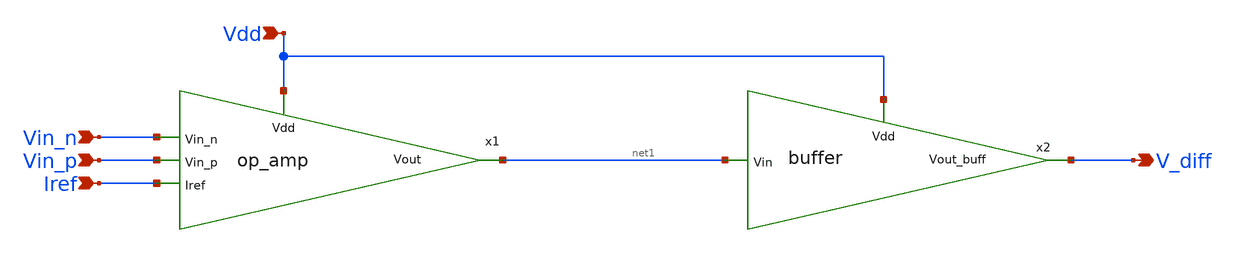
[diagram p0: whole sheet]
** sch_path: blocks/adc/lvds/lvds_rec_v3.sch
**.subckt lvds_rec_v3 Vin_p Vin_n V_diff Iref Vdd
*.ipin Vin_p
*.ipin Vin_n
*.opin V_diff
*.ipin Iref
*.ipin Vdd
x1 Vdd net1 Vin_n Vin_p Iref op_amp
x2 Vdd V_diff net1 buffer
**.ends

* expanding   symbol:  op_amp.sym # of pins=5
** sym_path: blocks/adc/lvds/op_amp.sym
** sch_path: blocks/adc/lvds/op_amp.sch
.subckt op_amp Vdd Vout Vin_n Vin_p Iref
*.ipin Vdd
*.ipin Vin_p
*.ipin Vin_n
*.opin Vout
*.ipin Iref
XM1 net2 net3 Vdd Vdd pfet_03v3 L=0.28u W=10.5u nf=1 ad='int((nf+1)/2) * W/nf * 0.18u' as='int((nf+2)/2) * W/nf * 0.18u'
+ pd='2*int((nf+1)/2) * (W/nf + 0.18u)' ps='2*int((nf+2)/2) * (W/nf + 0.18u)' nrd='0.18u / W' nrs='0.18u / W'
+ sa=0 sb=0 sd=0 m=1
XM2 net1 net4 Vdd Vdd pfet_03v3 L=0.28u W=10.5u nf=1 ad='int((nf+1)/2) * W/nf * 0.18u' as='int((nf+2)/2) * W/nf * 0.18u'
+ pd='2*int((nf+1)/2) * (W/nf + 0.18u)' ps='2*int((nf+2)/2) * (W/nf + 0.18u)' nrd='0.18u / W' nrs='0.18u / W'
+ sa=0 sb=0 sd=0 m=1
XM3 net3 Vb2 net2 Vdd pfet_03v3 L=0.28u W=10.5u nf=1 ad='int((nf+1)/2) * W/nf * 0.18u' as='int((nf+2)/2) * W/nf * 0.18u'
+ pd='2*int((nf+1)/2) * (W/nf + 0.18u)' ps='2*int((nf+2)/2) * (W/nf + 0.18u)' nrd='0.18u / W' nrs='0.18u / W'
+ sa=0 sb=0 sd=0 m=1
XM4 net4 Vb2 net1 Vdd pfet_03v3 L=0.28u W=10.5u nf=1 ad='int((nf+1)/2) * W/nf * 0.18u' as='int((nf+2)/2) * W/nf * 0.18u'
+ pd='2*int((nf+1)/2) * (W/nf + 0.18u)' ps='2*int((nf+2)/2) * (W/nf + 0.18u)' nrd='0.18u / W' nrs='0.18u / W'
+ sa=0 sb=0 sd=0 m=1
XM5 net4 Vin_p net5 0 nfet_03v3 L=0.28u W=52.5u nf=15 ad='int((nf+1)/2) * W/nf * 0.18u' as='int((nf+2)/2) * W/nf * 0.18u'
+ pd='2*int((nf+1)/2) * (W/nf + 0.18u)' ps='2*int((nf+2)/2) * (W/nf + 0.18u)' nrd='0.18u / W' nrs='0.18u / W'
+ sa=0 sb=0 sd=0 m=1
XM6 net3 Vin_n net5 0 nfet_03v3 L=0.28u W=52.5u nf=15 ad='int((nf+1)/2) * W/nf * 0.18u' as='int((nf+2)/2) * W/nf * 0.18u'
+ pd='2*int((nf+1)/2) * (W/nf + 0.18u)' ps='2*int((nf+2)/2) * (W/nf + 0.18u)' nrd='0.18u / W' nrs='0.18u / W'
+ sa=0 sb=0 sd=0 m=1
XM7 net6 net4 Vdd Vdd pfet_03v3 L=0.28u W=10.5u nf=1 ad='int((nf+1)/2) * W/nf * 0.18u' as='int((nf+2)/2) * W/nf * 0.18u'
+ pd='2*int((nf+1)/2) * (W/nf + 0.18u)' ps='2*int((nf+2)/2) * (W/nf + 0.18u)' nrd='0.18u / W' nrs='0.18u / W'
+ sa=0 sb=0 sd=0 m=1
XM9 net7 net3 Vdd Vdd pfet_03v3 L=0.28u W=10.5u nf=1 ad='int((nf+1)/2) * W/nf * 0.18u' as='int((nf+2)/2) * W/nf * 0.18u'
+ pd='2*int((nf+1)/2) * (W/nf + 0.18u)' ps='2*int((nf+2)/2) * (W/nf + 0.18u)' nrd='0.18u / W' nrs='0.18u / W'
+ sa=0 sb=0 sd=0 m=1
XM11 net8 Vb2 net10 0 nfet_03v3 L=0.28u W=5.25u nf=1 ad='int((nf+1)/2) * W/nf * 0.18u' as='int((nf+2)/2) * W/nf * 0.18u'
+ pd='2*int((nf+1)/2) * (W/nf + 0.18u)' ps='2*int((nf+2)/2) * (W/nf + 0.18u)' nrd='0.18u / W' nrs='0.18u / W'
+ sa=0 sb=0 sd=0 m=1
XM12 Vout Vb2 net9 0 nfet_03v3 L=0.28u W=5.25u nf=1 ad='int((nf+1)/2) * W/nf * 0.18u' as='int((nf+2)/2) * W/nf * 0.18u'
+ pd='2*int((nf+1)/2) * (W/nf + 0.18u)' ps='2*int((nf+2)/2) * (W/nf + 0.18u)' nrd='0.18u / W' nrs='0.18u / W'
+ sa=0 sb=0 sd=0 m=1
XM13 net10 net8 0 0 nfet_03v3 L=0.28u W=5.25u nf=1 ad='int((nf+1)/2) * W/nf * 0.18u' as='int((nf+2)/2) * W/nf * 0.18u'
+ pd='2*int((nf+1)/2) * (W/nf + 0.18u)' ps='2*int((nf+2)/2) * (W/nf + 0.18u)' nrd='0.18u / W' nrs='0.18u / W'
+ sa=0 sb=0 sd=0 m=1
XM14 net9 net8 0 0 nfet_03v3 L=0.28u W=5.25u nf=1 ad='int((nf+1)/2) * W/nf * 0.18u' as='int((nf+2)/2) * W/nf * 0.18u'
+ pd='2*int((nf+1)/2) * (W/nf + 0.18u)' ps='2*int((nf+2)/2) * (W/nf + 0.18u)' nrd='0.18u / W' nrs='0.18u / W'
+ sa=0 sb=0 sd=0 m=1
XM8 net8 0 net6 Vdd pfet_03v3 L=0.28u W=10.5u nf=1 ad='int((nf+1)/2) * W/nf * 0.18u' as='int((nf+2)/2) * W/nf * 0.18u'
+ pd='2*int((nf+1)/2) * (W/nf + 0.18u)' ps='2*int((nf+2)/2) * (W/nf + 0.18u)' nrd='0.18u / W' nrs='0.18u / W'
+ sa=0 sb=0 sd=0 m=1
XM10 Vout 0 net7 Vdd pfet_03v3 L=0.28u W=10.5u nf=1 ad='int((nf+1)/2) * W/nf * 0.18u' as='int((nf+2)/2) * W/nf * 0.18u'
+ pd='2*int((nf+1)/2) * (W/nf + 0.18u)' ps='2*int((nf+2)/2) * (W/nf + 0.18u)' nrd='0.18u / W' nrs='0.18u / W'
+ sa=0 sb=0 sd=0 m=1
XM15 net5 net11 0 0 nfet_03v3 L=1u W=80u nf=20 ad='int((nf+1)/2) * W/nf * 0.18u' as='int((nf+2)/2) * W/nf * 0.18u'
+ pd='2*int((nf+1)/2) * (W/nf + 0.18u)' ps='2*int((nf+2)/2) * (W/nf + 0.18u)' nrd='0.18u / W' nrs='0.18u / W'
+ sa=0 sb=0 sd=0 m=1
XM16 Iref Iref Vdd Vdd pfet_03v3 L=1u W=20u nf=1 ad='int((nf+1)/2) * W/nf * 0.18u' as='int((nf+2)/2) * W/nf * 0.18u'
+ pd='2*int((nf+1)/2) * (W/nf + 0.18u)' ps='2*int((nf+2)/2) * (W/nf + 0.18u)' nrd='0.18u / W' nrs='0.18u / W'
+ sa=0 sb=0 sd=0 m=1
XM17 net11 Iref Vdd Vdd pfet_03v3 L=1u W=80u nf=1 ad='int((nf+1)/2) * W/nf * 0.18u' as='int((nf+2)/2) * W/nf * 0.18u'
+ pd='2*int((nf+1)/2) * (W/nf + 0.18u)' ps='2*int((nf+2)/2) * (W/nf + 0.18u)' nrd='0.18u / W' nrs='0.18u / W'
+ sa=0 sb=0 sd=0 m=1
XM18 Vb2 Iref Vdd Vdd pfet_03v3 L=1u W=20u nf=1 ad='int((nf+1)/2) * W/nf * 0.18u' as='int((nf+2)/2) * W/nf * 0.18u'
+ pd='2*int((nf+1)/2) * (W/nf + 0.18u)' ps='2*int((nf+2)/2) * (W/nf + 0.18u)' nrd='0.18u / W' nrs='0.18u / W'
+ sa=0 sb=0 sd=0 m=1
XM19 Vb2 Vb2 net12 0 nfet_03v3 L=0.28u W=30u nf=1 ad='int((nf+1)/2) * W/nf * 0.18u' as='int((nf+2)/2) * W/nf * 0.18u'
+ pd='2*int((nf+1)/2) * (W/nf + 0.18u)' ps='2*int((nf+2)/2) * (W/nf + 0.18u)' nrd='0.18u / W' nrs='0.18u / W'
+ sa=0 sb=0 sd=0 m=1
XM20 net12 net12 0 0 nfet_03v3 L=0.28u W=30u nf=1 ad='int((nf+1)/2) * W/nf * 0.18u' as='int((nf+2)/2) * W/nf * 0.18u'
+ pd='2*int((nf+1)/2) * (W/nf + 0.18u)' ps='2*int((nf+2)/2) * (W/nf + 0.18u)' nrd='0.18u / W' nrs='0.18u / W'
+ sa=0 sb=0 sd=0 m=1
XM21 net11 net11 0 0 nfet_03v3 L=1u W=80u nf=1 ad='int((nf+1)/2) * W/nf * 0.18u' as='int((nf+2)/2) * W/nf * 0.18u'
+ pd='2*int((nf+1)/2) * (W/nf + 0.18u)' ps='2*int((nf+2)/2) * (W/nf + 0.18u)' nrd='0.18u / W' nrs='0.18u / W'
+ sa=0 sb=0 sd=0 m=1
.ends


* expanding   symbol:  buffer.sym # of pins=3
** sym_path: blocks/adc/lvds/buffer.sym
** sch_path: blocks/adc/lvds/buffer.sch
.subckt buffer Vdd Vout_buff Vin
*.ipin Vdd
*.ipin Vin
*.opin Vout_buff
XM1 net1 Vin Vdd Vdd pfet_03v3 L=0.28u W=0.66u nf=1 ad='int((nf+1)/2) * W/nf * 0.18u' as='int((nf+2)/2) * W/nf * 0.18u'
+ pd='2*int((nf+1)/2) * (W/nf + 0.18u)' ps='2*int((nf+2)/2) * (W/nf + 0.18u)' nrd='0.18u / W' nrs='0.18u / W'
+ sa=0 sb=0 sd=0 m=1
XM2 net1 Vin 0 0 nfet_03v3 L=0.28u W=0.22u nf=1 ad='int((nf+1)/2) * W/nf * 0.18u' as='int((nf+2)/2) * W/nf * 0.18u'
+ pd='2*int((nf+1)/2) * (W/nf + 0.18u)' ps='2*int((nf+2)/2) * (W/nf + 0.18u)' nrd='0.18u / W' nrs='0.18u / W'
+ sa=0 sb=0 sd=0 m=1
XM3 net2 net1 Vdd Vdd pfet_03v3 L=0.28u W=2.64u nf=1 ad='int((nf+1)/2) * W/nf * 0.18u' as='int((nf+2)/2) * W/nf * 0.18u'
+ pd='2*int((nf+1)/2) * (W/nf + 0.18u)' ps='2*int((nf+2)/2) * (W/nf + 0.18u)' nrd='0.18u / W' nrs='0.18u / W'
+ sa=0 sb=0 sd=0 m=1
XM4 net2 net1 0 0 nfet_03v3 L=0.28u W=0.88u nf=1 ad='int((nf+1)/2) * W/nf * 0.18u' as='int((nf+2)/2) * W/nf * 0.18u'
+ pd='2*int((nf+1)/2) * (W/nf + 0.18u)' ps='2*int((nf+2)/2) * (W/nf + 0.18u)' nrd='0.18u / W' nrs='0.18u / W'
+ sa=0 sb=0 sd=0 m=1
XM5 net3 net2 Vdd Vdd pfet_03v3 L=0.28u W=10.56u nf=1 ad='int((nf+1)/2) * W/nf * 0.18u' as='int((nf+2)/2) * W/nf * 0.18u'
+ pd='2*int((nf+1)/2) * (W/nf + 0.18u)' ps='2*int((nf+2)/2) * (W/nf + 0.18u)' nrd='0.18u / W' nrs='0.18u / W'
+ sa=0 sb=0 sd=0 m=1
XM6 net3 net2 0 0 nfet_03v3 L=0.28u W=3.52u nf=1 ad='int((nf+1)/2) * W/nf * 0.18u' as='int((nf+2)/2) * W/nf * 0.18u'
+ pd='2*int((nf+1)/2) * (W/nf + 0.18u)' ps='2*int((nf+2)/2) * (W/nf + 0.18u)' nrd='0.18u / W' nrs='0.18u / W'
+ sa=0 sb=0 sd=0 m=1
XM7 Vout_buff net3 Vdd Vdd pfet_03v3 L=0.28u W=45u nf=1 ad='int((nf+1)/2) * W/nf * 0.18u' as='int((nf+2)/2) * W/nf * 0.18u'
+ pd='2*int((nf+1)/2) * (W/nf + 0.18u)' ps='2*int((nf+2)/2) * (W/nf + 0.18u)' nrd='0.18u / W' nrs='0.18u / W'
+ sa=0 sb=0 sd=0 m=1
XM8 Vout_buff net3 0 0 nfet_03v3 L=0.28u W=14u nf=1 ad='int((nf+1)/2) * W/nf * 0.18u' as='int((nf+2)/2) * W/nf * 0.18u'
+ pd='2*int((nf+1)/2) * (W/nf + 0.18u)' ps='2*int((nf+2)/2) * (W/nf + 0.18u)' nrd='0.18u / W' nrs='0.18u / W'
+ sa=0 sb=0 sd=0 m=1
.ends

.end
